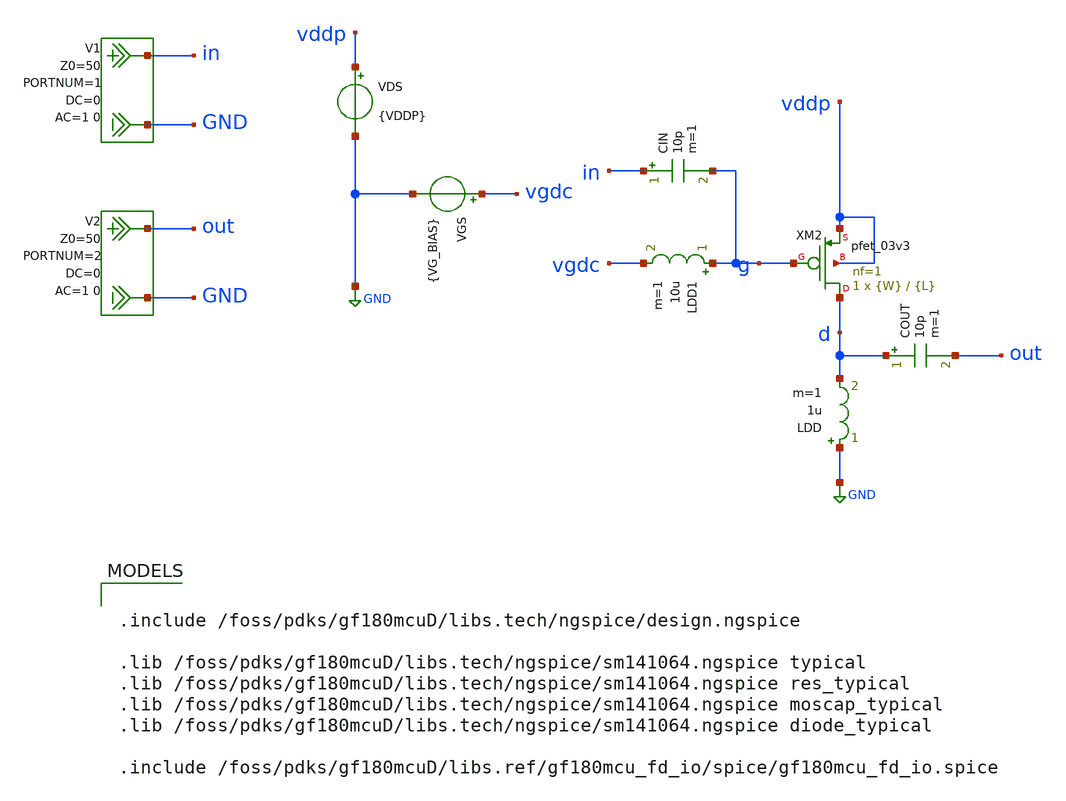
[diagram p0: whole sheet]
** sch_path: NFmin_Simulation/simulations/03v0/nfmin_jd_pmos.sch
**.subckt nfmin_jd_pmos
VGS vgdc GND {VG_BIAS}
VDS vddp GND {VDDP}
LDD GND d 1u m=1
COUT d out 10p m=1
CIN in g 10p m=1
XM2 d g vddp vddp pfet_03v3 L={L} W={W} nf=1 ad='int((nf+1)/2) * W/nf * 0.18u' as='int((nf+2)/2) * W/nf * 0.18u'
+ pd='2*int((nf+1)/2) * (W/nf + 0.18u)' ps='2*int((nf+2)/2) * (W/nf + 0.18u)' nrd='0.18u / W' nrs='0.18u / W'
+ sa=0 sb=0 sd=0 m=1
V1 in GND DC 0 AC 1 0 portnum 1 z0 50
V2 out GND DC 0 AC 1 0 portnum 2 z0 50
LDD1 g vgdc 10u m=1
**** begin user architecture code

.include /foss/pdks/gf180mcuD/libs.tech/ngspice/design.ngspice

.lib /foss/pdks/gf180mcuD/libs.tech/ngspice/sm141064.ngspice typical
.lib /foss/pdks/gf180mcuD/libs.tech/ngspice/sm141064.ngspice res_typical
.lib /foss/pdks/gf180mcuD/libs.tech/ngspice/sm141064.ngspice moscap_typical
.lib /foss/pdks/gf180mcuD/libs.tech/ngspice/sm141064.ngspice diode_typical

.include /foss/pdks/gf180mcuD/libs.ref/gf180mcu_fd_io/spice/gf180mcu_fd_io.spice



.option savecurrents

.param fnoicor=0
.param sw_stat_mismatch=0

* Default values
.param VDDP=1.8
.param VSG_BIAS=0.7
.param VG_BIAS={VDDP-VSG_BIAS}

.param W=0.22e-6
.param L=0.28e-6

.control
  set noaskquit
  save all

  echo W_m L_m VSG ID_A JD_mA_per_um > pmos_geom_jd.txt
  echo W_m L_m VSG NFmin_dB NF_dB Rn SOpt_real SOpt_imag > pmos_geom_nf.txt

  * Width sweep in meters:
  foreach wval 0.22e-6 1e-6 5e-6 10e-6

    * Length sweep in meters:
    foreach lval 0.28e-6 0.36e-6 0.50e-6

      * VSG sweep:
      * 0.35 V to 1.20 V in 5 mV steps
      let k = 0
      while k <= 170

        let vsg = 0.35 + 0.005*k

        alterparam W = $wval
        alterparam L = $lval
        alterparam VSG_BIAS = $&vsg
        reset

        op

        let idp_op = abs(i(vds))
        let jd_p_op = 1e-3*idp_op/$wval

        echo $wval $lval $&vsg $&idp_op $&jd_p_op >> pmos_geom_jd.txt

        sp lin 1 2.4e9 2.4e9 1

        let nfmin_val = real(NFmin)
        let nf_val = real(NF)
        let rn_val = real(Rn)
        let sopt_re = real(SOpt)
        let sopt_im = imag(SOpt)

        echo $wval $lval $&vsg $&nfmin_val $&nf_val $&rn_val $&sopt_re $&sopt_im >> pmos_geom_nf.txt

        let k = k + 1

      end

    end

  end

.endc



**** end user architecture code
**.ends
.GLOBAL GND
.end
